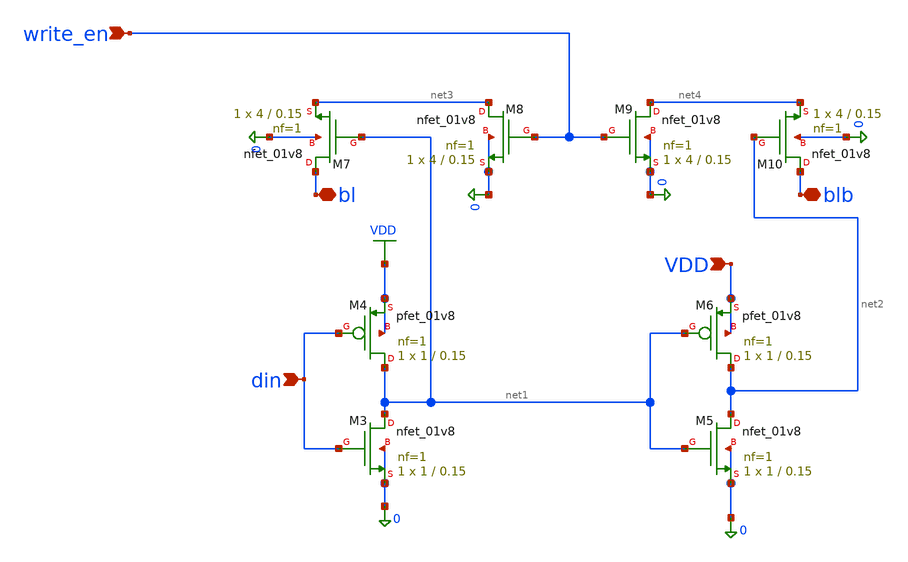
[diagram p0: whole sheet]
** sch_path: xschem/Subcircuits/write_driver.sch
**.subckt write_driver VDD write_en din bl blb
*.ipin VDD
*.ipin write_en
*.ipin din
*.iopin bl
*.iopin blb
XM3 net1 din 0 0 sky130_fd_pr__nfet_01v8 L=0.15 W=1 nf=1 ad='int((1 + 1)/2) * 1 / 1 * 0.29' as='int((1 + 2)/2) * 1 / 1 * 0.29'
+ pd='2*int((1 + 1)/2) * (1 / 1 + 0.29)' ps='2*int((1 + 2)/2) * (1 / 1 + 0.29)' nrd='0.29 / 1 ' nrs='0.29 / 1 '
+ sa=0 sb=0 sd=0 mult=1 m=1
XM4 net1 din VDD VDD sky130_fd_pr__pfet_01v8 L=0.15 W=1 nf=1 ad='int((1 + 1)/2) * 1 / 1 * 0.29' as='int((1 + 2)/2) * 1 / 1 * 0.29'
+ pd='2*int((1 + 1)/2) * (1 / 1 + 0.29)' ps='2*int((1 + 2)/2) * (1 / 1 + 0.29)' nrd='0.29 / 1 ' nrs='0.29 / 1 '
+ sa=0 sb=0 sd=0 mult=1 m=1
XM5 net2 net1 0 0 sky130_fd_pr__nfet_01v8 L=0.15 W=1 nf=1 ad='int((1 + 1)/2) * 1 / 1 * 0.29' as='int((1 + 2)/2) * 1 / 1 * 0.29'
+ pd='2*int((1 + 1)/2) * (1 / 1 + 0.29)' ps='2*int((1 + 2)/2) * (1 / 1 + 0.29)' nrd='0.29 / 1 ' nrs='0.29 / 1 '
+ sa=0 sb=0 sd=0 mult=1 m=1
XM6 net2 net1 VDD VDD sky130_fd_pr__pfet_01v8 L=0.15 W=1 nf=1 ad='int((1 + 1)/2) * 1 / 1 * 0.29' as='int((1 + 2)/2) * 1 / 1 * 0.29'
+ pd='2*int((1 + 1)/2) * (1 / 1 + 0.29)' ps='2*int((1 + 2)/2) * (1 / 1 + 0.29)' nrd='0.29 / 1 ' nrs='0.29 / 1 '
+ sa=0 sb=0 sd=0 mult=1 m=1
XM8 net3 write_en 0 0 sky130_fd_pr__nfet_01v8 L=0.15 W=4 nf=1 ad='int((1 + 1)/2) * 4 / 1 * 0.29' as='int((1 + 2)/2) * 4 / 1 * 0.29'
+ pd='2*int((1 + 1)/2) * (4 / 1 + 0.29)' ps='2*int((1 + 2)/2) * (4 / 1 + 0.29)' nrd='0.29 / 4 ' nrs='0.29 / 4 '
+ sa=0 sb=0 sd=0 mult=1 m=1
XM9 net4 write_en 0 0 sky130_fd_pr__nfet_01v8 L=0.15 W=4 nf=1 ad='int((1 + 1)/2) * 4 / 1 * 0.29' as='int((1 + 2)/2) * 4 / 1 * 0.29'
+ pd='2*int((1 + 1)/2) * (4 / 1 + 0.29)' ps='2*int((1 + 2)/2) * (4 / 1 + 0.29)' nrd='0.29 / 4 ' nrs='0.29 / 4 '
+ sa=0 sb=0 sd=0 mult=1 m=1
XM7 bl net1 net3 0 sky130_fd_pr__nfet_01v8 L=0.15 W=4 nf=1 ad='int((1 + 1)/2) * 4 / 1 * 0.29' as='int((1 + 2)/2) * 4 / 1 * 0.29'
+ pd='2*int((1 + 1)/2) * (4 / 1 + 0.29)' ps='2*int((1 + 2)/2) * (4 / 1 + 0.29)' nrd='0.29 / 4 ' nrs='0.29 / 4 '
+ sa=0 sb=0 sd=0 mult=1 m=1
XM10 blb net2 net4 0 sky130_fd_pr__nfet_01v8 L=0.15 W=4 nf=1 ad='int((1 + 1)/2) * 4 / 1 * 0.29' as='int((1 + 2)/2) * 4 / 1 * 0.29'
+ pd='2*int((1 + 1)/2) * (4 / 1 + 0.29)' ps='2*int((1 + 2)/2) * (4 / 1 + 0.29)' nrd='0.29 / 4 ' nrs='0.29 / 4 '
+ sa=0 sb=0 sd=0 mult=1 m=1
**.ends
.GLOBAL VDD
.end
